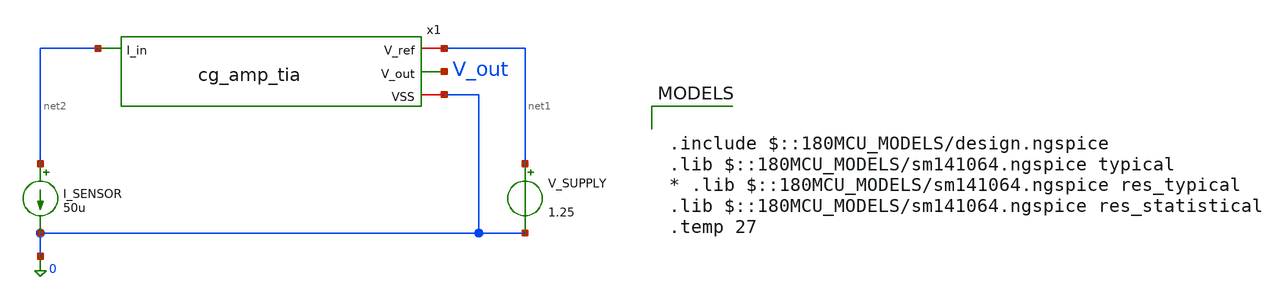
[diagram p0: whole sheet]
** sch_path: lvs/schematics/tb_cg_amp_tia.sch
**.subckt tb_cg_amp_tia
x1 net1 V_out net2 0 cg_amp_tia
V_SUPPLY net1 0 1.25
I_SENSOR net2 0 50u
**** begin user architecture code

.include $::180MCU_MODELS/design.ngspice
.lib $::180MCU_MODELS/sm141064.ngspice typical
* .lib $::180MCU_MODELS/sm141064.ngspice res_typical
.lib $::180MCU_MODELS/sm141064.ngspice res_statistical
.temp 27



.control
  op
  print v(V_out)
  print @m.x1.xm1.m0[vgs] @m.x1.xm1.m0[vth] @m.x1.xm1.m0[vdsat] @m.x1.xm1.m0[id] @m.x1.xm1.m0[gm]
+ @m.x1.xm1.m0[gds]
  print @r.x1.xr1.rt1[resistance] @r.x1.xr1.rt2[resistance]

  dc I_SENSOR 0 50u 1u
  let V_out_swp = v(V_out)
  plot V_out_swp title "CG-TIA: Sensor Current to Voltage"
  wrdata /foss/designs/analog-perceptron-gf180mcu/plots/cg_amp_tia_sweep.txt V_out_swp
  * === OP-SWEEP DIAGNOSTIC: M1 headroom across full 0-50uA input range ===
  save all @m.x1.xm1.m0[vgs] @m.x1.xm1.m0[vth] @m.x1.xm1.m0[vdsat] @m.x1.xm1.m0[id] @m.x1.xm1.m0[gm]
+ @m.x1.xm1.m0[gds]
  dc I_SENSOR 0 50u 1u
  wrdata /foss/designs/analog-perceptron-gf180mcu/plots/opsweep_cg_amp_tia.txt v(V_out)
+ @m.x1.xm1.m0[vgs] @m.x1.xm1.m0[vth] @m.x1.xm1.m0[vdsat] @m.x1.xm1.m0[id] @m.x1.xm1.m0[gm] @m.x1.xm1.m0[gds]
.endc


**** end user architecture code
**.ends
.end
